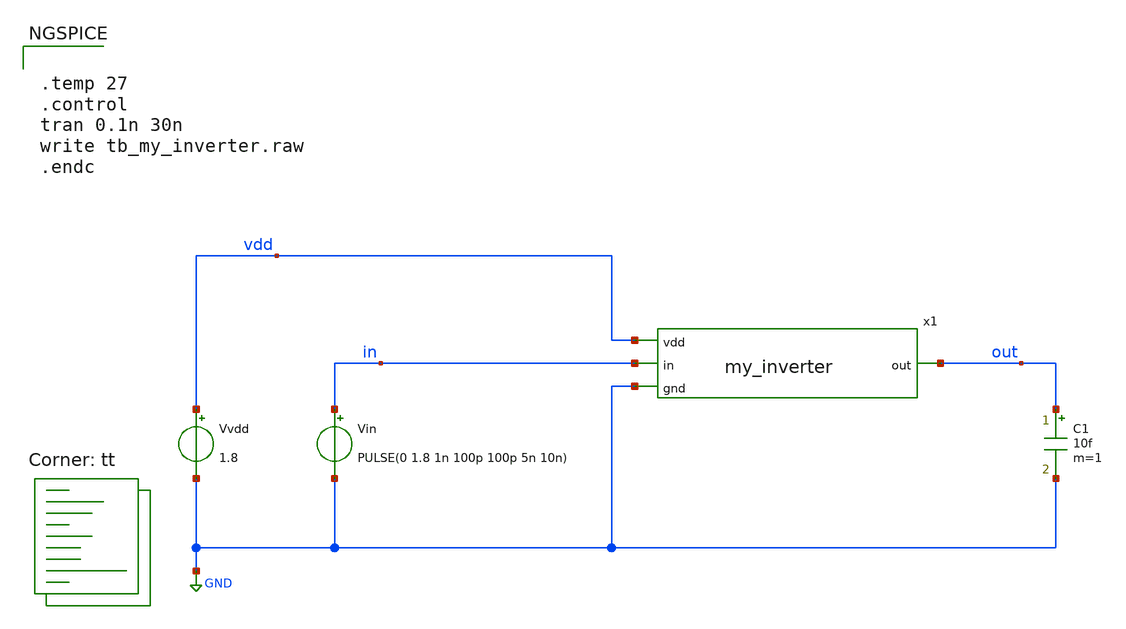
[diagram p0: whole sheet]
** sch_path: examples/analog/tb_my_inverter.sch
**.subckt tb_my_inverter
Vvdd vdd GND 1.8
Vin in GND PULSE(0 1.8 1n 100p 100p 5n 10n)
x1 vdd in out GND my_inverter
C1 out GND 10f m=1
**** begin user architecture code
.lib $::SKYWATER_MODELS/sky130.lib.spice tt


.temp 27
.control
tran 0.1n 30n
write tb_my_inverter.raw
.endc


**** end user architecture code
**.ends

* expanding   symbol:  my_inverter.sym # of pins=4
** sym_path: examples/analog/my_inverter.sym
** sch_path: examples/analog/my_inverter.sch
.subckt my_inverter vdd in out gnd
*.ipin in
*.opin out
*.iopin vdd
*.iopin gnd
XM1 out in vdd vdd sky130_fd_pr__pfet_01v8 L=0.15 W=2 nf=1 ad='int((nf+1)/2) * W/nf * 0.29' as='int((nf+2)/2) * W/nf * 0.29'
+ pd='2*int((nf+1)/2) * (W/nf + 0.29)' ps='2*int((nf+2)/2) * (W/nf + 0.29)' nrd='0.29 / W' nrs='0.29 / W'
+ sa=0 sb=0 sd=0 mult=1 m=1
XM2 out in gnd gnd sky130_fd_pr__nfet_01v8 L=0.15 W=1 nf=1 ad='int((1 + 1)/2) * 1 / 1 * 0.29' as='int((1 + 2)/2) * 1 / 1 * 0.29'
+ pd='2*int((1 + 1)/2) * (1 / 1 + 0.29)' ps='2*int((1 + 2)/2) * (1 / 1 + 0.29)' nrd='0.29 / 1 ' nrs='0.29 / 1 '
+ sa=0 sb=0 sd=0 mult=1 m=1
.ends

.GLOBAL GND
.end
